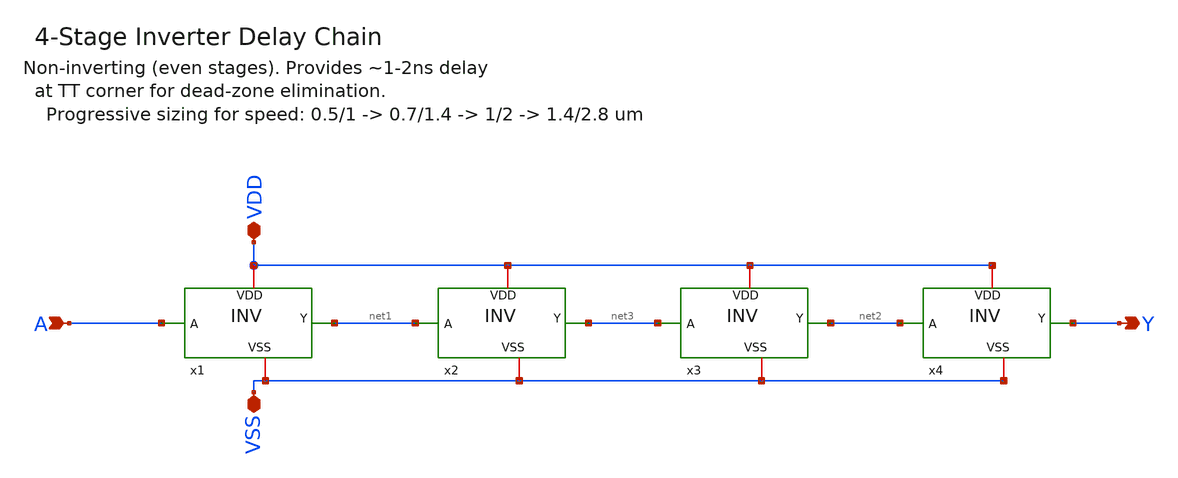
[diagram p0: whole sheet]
** sch_path: designs/libs/core_analog/pfd/leftover_files/delay_chain.sch
**.subckt delay_chain A Y VDD VSS
*.ipin A
*.opin Y
*.iopin VDD
*.iopin VSS
x1 VDD net1 A VSS inv
x2 VDD net3 net1 VSS inv
x3 VDD net2 net3 VSS inv
x4 VDD Y net2 VSS inv
**.ends
.end
